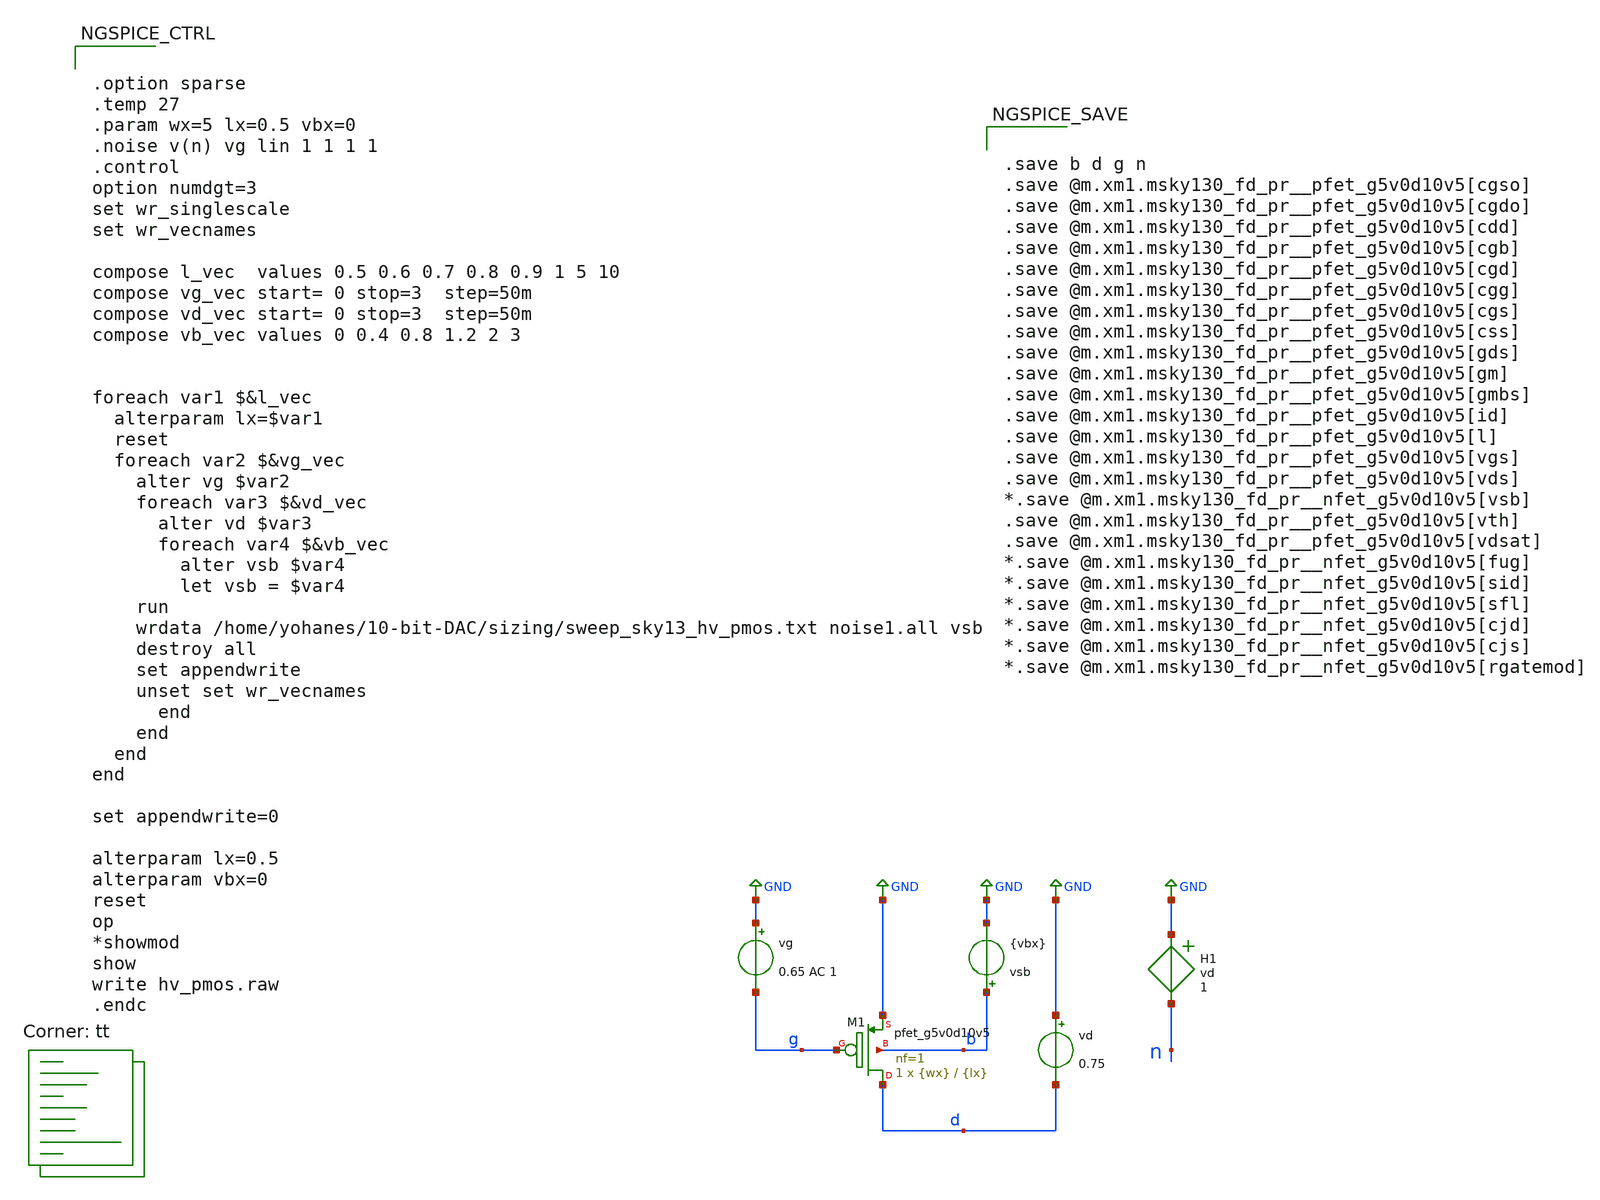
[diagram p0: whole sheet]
** sch_path: xschem/hv_pmos-tb.sch
* (c) 2024 H. Pretl, Apache-2.0 license (adapted from B. Murmann)
**.subckt hv_pmos-tb
vd GND d 0.75
vsb b GND {vbx}
vg GND g 0.65 AC 1
H1 GND n vd 1
XM1 d g GND b sky130_fd_pr__pfet_g5v0d10v5 L={lx} W={wx} nf=1 ad='int((nf+1)/2) * W/nf * 0.29' as='int((nf+2)/2) * W/nf * 0.29'
+ pd='2*int((nf+1)/2) * (W/nf + 0.29)' ps='2*int((nf+2)/2) * (W/nf + 0.29)' nrd='0.29 / W' nrs='0.29 / W'
+ sa=0 sb=0 sd=0 mult=1 m=1
**** begin user architecture code


.option sparse
.temp 27
.param wx=5 lx=0.5 vbx=0
.noise v(n) vg lin 1 1 1 1
.control
option numdgt=3
set wr_singlescale
set wr_vecnames

compose l_vec  values 0.5 0.6 0.7 0.8 0.9 1 5 10
compose vg_vec start= 0 stop=3  step=50m
compose vd_vec start= 0 stop=3  step=50m
compose vb_vec values 0 0.4 0.8 1.2 2 3


foreach var1 $&l_vec
  alterparam lx=$var1
  reset
  foreach var2 $&vg_vec
    alter vg $var2
    foreach var3 $&vd_vec
      alter vd $var3
      foreach var4 $&vb_vec
        alter vsb $var4
        let vsb = $var4
	run
	wrdata /home/yohanes/10-bit-DAC/sizing/sweep_sky13_hv_pmos.txt noise1.all vsb
	destroy all
	set appendwrite
	unset set wr_vecnames
      end
    end
  end
end

set appendwrite=0

alterparam lx=0.5
alterparam vbx=0
reset
op
*showmod
show
write hv_pmos.raw
.endc




.save b d g n
.save @m.xm1.msky130_fd_pr__pfet_g5v0d10v5[cgso]
.save @m.xm1.msky130_fd_pr__pfet_g5v0d10v5[cgdo]
.save @m.xm1.msky130_fd_pr__pfet_g5v0d10v5[cdd]
.save @m.xm1.msky130_fd_pr__pfet_g5v0d10v5[cgb]
.save @m.xm1.msky130_fd_pr__pfet_g5v0d10v5[cgd]
.save @m.xm1.msky130_fd_pr__pfet_g5v0d10v5[cgg]
.save @m.xm1.msky130_fd_pr__pfet_g5v0d10v5[cgs]
.save @m.xm1.msky130_fd_pr__pfet_g5v0d10v5[css]
.save @m.xm1.msky130_fd_pr__pfet_g5v0d10v5[gds]
.save @m.xm1.msky130_fd_pr__pfet_g5v0d10v5[gm]
.save @m.xm1.msky130_fd_pr__pfet_g5v0d10v5[gmbs]
.save @m.xm1.msky130_fd_pr__pfet_g5v0d10v5[id]
.save @m.xm1.msky130_fd_pr__pfet_g5v0d10v5[l]
.save @m.xm1.msky130_fd_pr__pfet_g5v0d10v5[vgs]
.save @m.xm1.msky130_fd_pr__pfet_g5v0d10v5[vds]
*.save @m.xm1.msky130_fd_pr__nfet_g5v0d10v5[vsb]
.save @m.xm1.msky130_fd_pr__pfet_g5v0d10v5[vth]
.save @m.xm1.msky130_fd_pr__pfet_g5v0d10v5[vdsat]
*.save @m.xm1.msky130_fd_pr__nfet_g5v0d10v5[fug]
*.save @m.xm1.msky130_fd_pr__nfet_g5v0d10v5[sid]
*.save @m.xm1.msky130_fd_pr__nfet_g5v0d10v5[sfl]
*.save @m.xm1.msky130_fd_pr__nfet_g5v0d10v5[cjd]
*.save @m.xm1.msky130_fd_pr__nfet_g5v0d10v5[cjs]
*.save @m.xm1.msky130_fd_pr__nfet_g5v0d10v5[rgatemod]


.lib $::SKYWATER_MODELS/sky130.lib.spice tt
**** end user architecture code
**.ends
.GLOBAL GND
.end
